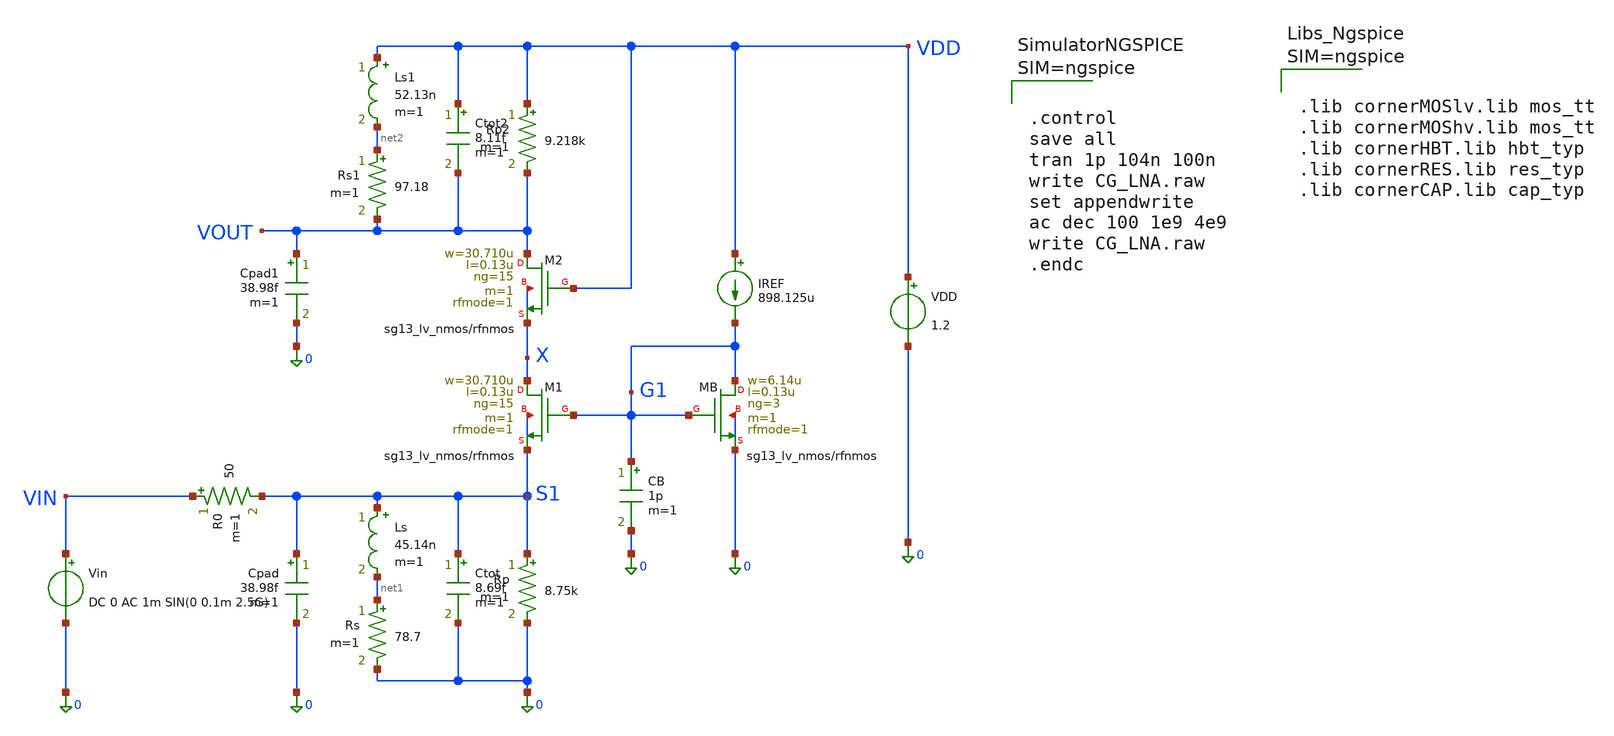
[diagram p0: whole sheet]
** sch_path: xschem/CG_LNA.sch
**.subckt CG_LNA
XM1 X G1 S1 S1 sg13_lv_nmos w=30.710u l=0.13u ng=15 m=1 rfmode=1 mm_ok=1
XM2 VOUT VDD X X sg13_lv_nmos w=30.710u l=0.13u ng=15 m=1 rfmode=1 mm_ok=1
XMB G1 G1 0 0 sg13_lv_nmos w=6.14u l=0.13u ng=3 m=1 rfmode=1 mm_ok=1
CB G1 0 1p m=1
Rp S1 0 8.75k m=1
Ls S1 net1 45.14n m=1
Ctot S1 0 8.69f m=1
IREF VDD G1 898.125u
Rs net1 0 78.7 m=1
Vin VIN 0 DC 0 AC 1m SIN(0 0.1m 2.5G)
R0 VIN S1 50 m=1
Cpad S1 0 38.98f m=1
Rp2 VDD VOUT 9.218k m=1
Ls1 VDD net2 52.13n m=1
Ctot2 VDD VOUT 8.11f m=1
Rs1 net2 VOUT 97.18 m=1
Cpad1 VOUT 0 38.98f m=1
VDD VDD 0 1.2
**** begin user architecture code



.lib cornerMOSlv.lib mos_tt
.lib cornerMOShv.lib mos_tt
.lib cornerHBT.lib hbt_typ
.lib cornerRES.lib res_typ
.lib cornerCAP.lib cap_typ






.control
save all
tran 1p 104n 100n
write CG_LNA.raw
set appendwrite
ac dec 100 1e9 4e9
write CG_LNA.raw
.endc



**** end user architecture code
**.ends
.end
